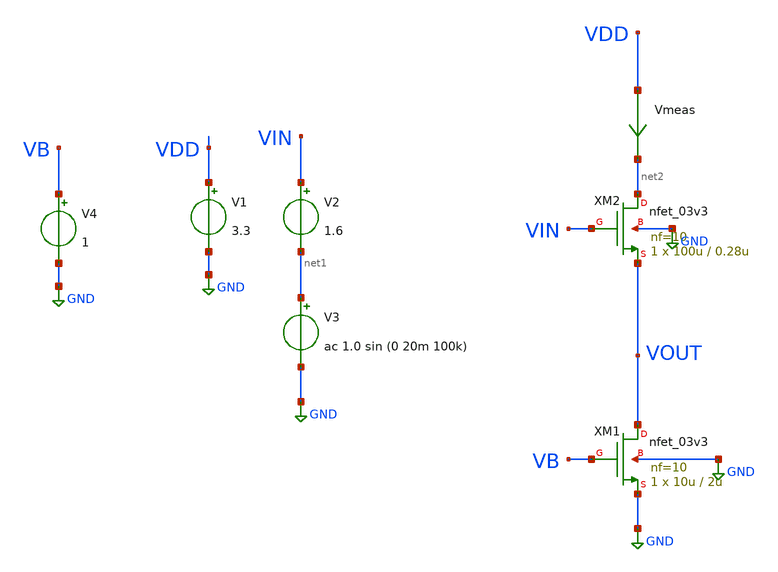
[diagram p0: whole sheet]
** sch_path: simple_amp11.sch
**.subckt simple_amp11
XM1 VOUT VB GND GND nfet_03v3 L=2u W=10u nf=10 ad='int((nf+1)/2) * W/nf * 0.18u' as='int((nf+2)/2) * W/nf * 0.18u'
+ pd='2*int((nf+1)/2) * (W/nf + 0.18u)' ps='2*int((nf+2)/2) * (W/nf + 0.18u)' nrd='0.18u / W' nrs='0.18u / W'
+ sa=0 sb=0 sd=0 m=1
Vmeas VDD net2 0
.save i(vmeas)
V1 VDD GND 3.3
V2 VIN net1 1.6
V3 net1 GND ac 1.0 sin (0 20m 100k)
V4 VB GND 1
XM2 net2 VIN VOUT GND nfet_03v3 L=0.28u W=100u nf=10 ad='int((nf+1)/2) * W/nf * 0.18u' as='int((nf+2)/2) * W/nf * 0.18u'
+ pd='2*int((nf+1)/2) * (W/nf + 0.18u)' ps='2*int((nf+2)/2) * (W/nf + 0.18u)' nrd='0.18u / W' nrs='0.18u / W'
+ sa=0 sb=0 sd=0 m=1
**** begin user architecture code

.include $::180MCU_MODELS/design.ngspice
*.lib $::180MCU_MODELS/sm141064.ngspice statistical
*.lib $::180MCU_MODELS/sm141064.ngspice res_statistical
.lib $::180MCU_MODELS/sm141064.ngspice typical
.lib $::180MCU_MODELS/sm141064.ngspice res_typical
.lib $::180MCU_MODELS/sm141064.ngspice moscap_typical
.lib $::180MCU_MODELS/sm141064.ngspice bjt_typical
.lib $::180MCU_MODELS/sm141064.ngspice diode_typical
.lib $::180MCU_MODELS/sm141064.ngspice mimcap_typical
.TEMP 27

.param   sw_stat_global = 1   sw_stat_mism = 1  mc_skew = 3  res_mc_skew = 3  cap_mc_skew = 3
+  fnoicor = 1



.control
save all
dc V2 0 3.3 0.01


plot v(VOUT) deriv(v(VOUT)) v(VIN)
plot deriv(v(VOUT)) (v(VDD)-v(VG)) (v(VDD)-v(VOUT))
plot i(Vmeas)
plot deriv(v(VOUT))
tran 10ns 20u
plot (v(VOUT)-0.942) (v(VIN)-1.6)
plot fft((v(VOUT))) fft((v(VIN)))
ac dec 20 1 50G
plot v(VOUT)
.endc

**** end user architecture code
**.ends
.GLOBAL GND
.end
